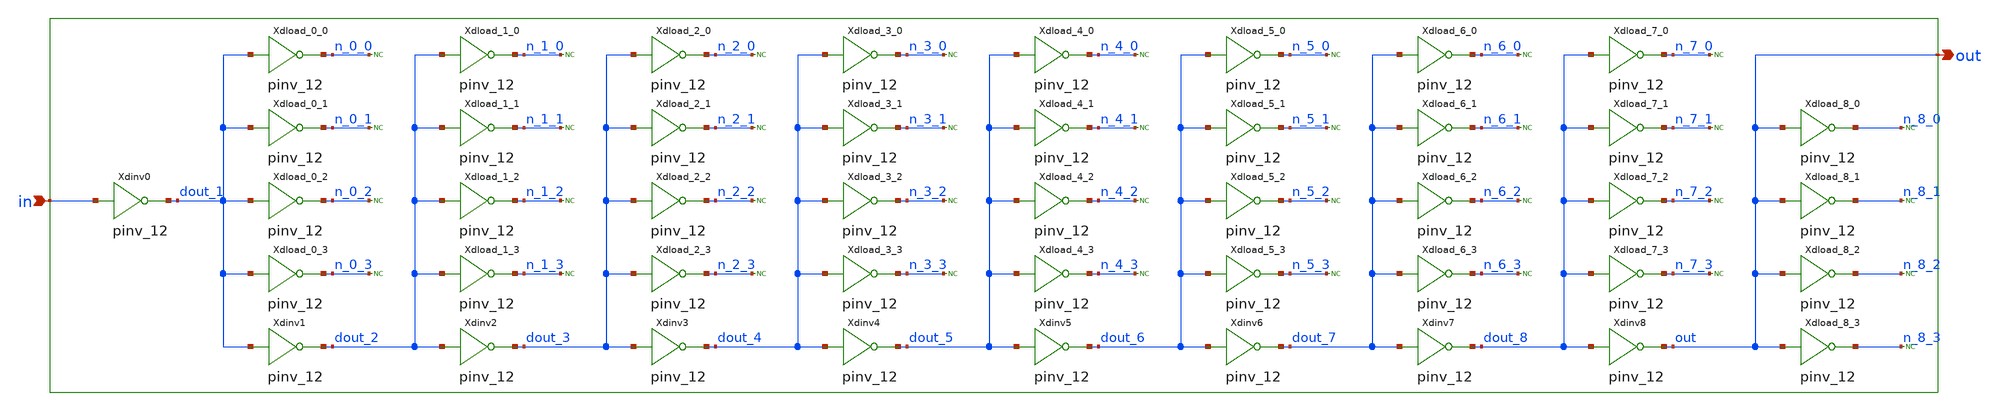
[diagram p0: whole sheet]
** sch_path: sram_4_16_scn4m/delay_chain.sch
**.subckt delay_chain in out
*.ipin in
*.opin out
Xdinv0 in dout_1 gnd gnd pinv_12
Xdload_0_0 dout_1 n_0_0 gnd gnd pinv_12
Xdload_0_1 dout_1 n_0_1 gnd gnd pinv_12
Xdload_0_2 dout_1 n_0_2 gnd gnd pinv_12
Xdload_0_3 dout_1 n_0_3 gnd gnd pinv_12
Xdinv1 dout_1 dout_2 gnd gnd pinv_12
Xdload_1_0 dout_2 n_1_0 gnd gnd pinv_12
Xdload_1_1 dout_2 n_1_1 gnd gnd pinv_12
Xdload_1_2 dout_2 n_1_2 gnd gnd pinv_12
Xdload_1_3 dout_2 n_1_3 gnd gnd pinv_12
Xdinv2 dout_2 dout_3 gnd gnd pinv_12
Xdload_2_0 dout_3 n_2_0 gnd gnd pinv_12
Xdload_2_1 dout_3 n_2_1 gnd gnd pinv_12
Xdload_2_2 dout_3 n_2_2 gnd gnd pinv_12
Xdload_2_3 dout_3 n_2_3 gnd gnd pinv_12
Xdinv3 dout_3 dout_4 gnd gnd pinv_12
Xdload_3_0 dout_4 n_3_0 gnd gnd pinv_12
Xdload_3_1 dout_4 n_3_1 gnd gnd pinv_12
Xdload_3_2 dout_4 n_3_2 gnd gnd pinv_12
Xdload_3_3 dout_4 n_3_3 gnd gnd pinv_12
Xdinv4 dout_4 dout_5 gnd gnd pinv_12
Xdload_4_0 dout_5 n_4_0 gnd gnd pinv_12
Xdload_4_1 dout_5 n_4_1 gnd gnd pinv_12
Xdload_4_2 dout_5 n_4_2 gnd gnd pinv_12
Xdload_4_3 dout_5 n_4_3 gnd gnd pinv_12
Xdinv5 dout_5 dout_6 gnd gnd pinv_12
Xdload_5_0 dout_6 n_5_0 gnd gnd pinv_12
Xdload_5_1 dout_6 n_5_1 gnd gnd pinv_12
Xdload_5_2 dout_6 n_5_2 gnd gnd pinv_12
Xdload_5_3 dout_6 n_5_3 gnd gnd pinv_12
Xdinv6 dout_6 dout_7 gnd gnd pinv_12
Xdload_6_0 dout_7 n_6_0 gnd gnd pinv_12
Xdload_6_1 dout_7 n_6_1 gnd gnd pinv_12
Xdload_6_2 dout_7 n_6_2 gnd gnd pinv_12
Xdload_6_3 dout_7 n_6_3 gnd gnd pinv_12
Xdinv7 dout_7 dout_8 gnd gnd pinv_12
Xdload_7_0 dout_8 n_7_0 gnd gnd pinv_12
Xdload_7_1 dout_8 n_7_1 gnd gnd pinv_12
Xdload_7_2 dout_8 n_7_2 gnd gnd pinv_12
Xdload_7_3 dout_8 n_7_3 gnd gnd pinv_12
Xdinv8 dout_8 out gnd gnd pinv_12
Xdload_8_0 out n_8_0 gnd gnd pinv_12
Xdload_8_1 out n_8_1 gnd gnd pinv_12
Xdload_8_2 out n_8_2 gnd gnd pinv_12
Xdload_8_3 out n_8_3 gnd gnd pinv_12
* noconn n_0_0
* noconn n_0_1
* noconn n_0_2
* noconn n_0_3
* noconn n_1_0
* noconn n_1_1
* noconn n_1_2
* noconn n_1_3
* noconn n_2_0
* noconn n_2_1
* noconn n_2_2
* noconn n_2_3
* noconn n_3_0
* noconn n_3_1
* noconn n_3_2
* noconn n_3_3
* noconn n_4_0
* noconn n_4_1
* noconn n_4_2
* noconn n_4_3
* noconn n_5_0
* noconn n_5_1
* noconn n_5_2
* noconn n_5_3
* noconn n_6_0
* noconn n_6_1
* noconn n_6_2
* noconn n_6_3
* noconn n_7_0
* noconn n_7_1
* noconn n_7_2
* noconn n_7_3
* noconn n_8_0
* noconn n_8_1
* noconn n_8_2
* noconn n_8_3
**.ends

* expanding   symbol:  pinv_12.sym # of pins=2
** sym_path: sram_2_64_scn4m/pinv_12.sym
** sch_path: sram_2_64_scn4m/pinv_12.sch
.subckt pinv_12 A Z vdd gnd
*.ipin A
*.opin Z
*.iopin vdd
*.iopin gnd
XM2 Z A gnd gnd sky130_fd_pr__nfet_01v8 L=0.4 W=4.0 nf=1 ad='int((nf+1)/2) * W/nf * 0.29' as='int((nf+2)/2) * W/nf * 0.29'
+ pd='2*int((nf+1)/2) * (W/nf + 0.29)' ps='2*int((nf+2)/2) * (W/nf + 0.29)' nrd='0.29 / W' nrs='0.29 / W'
+ sa=0 sb=0 sd=0 mult=2 m=2
XM3 Z A vdd vdd sky130_fd_pr__pfet_01v8 L=0.4 W=8.0 nf=1 ad='int((nf+1)/2) * W/nf * 0.29' as='int((nf+2)/2) * W/nf * 0.29'
+ pd='2*int((nf+1)/2) * (W/nf + 0.29)' ps='2*int((nf+2)/2) * (W/nf + 0.29)' nrd='0.29 / W' nrs='0.29 / W'
+ sa=0 sb=0 sd=0 mult=2 m=2
.ends

.end
